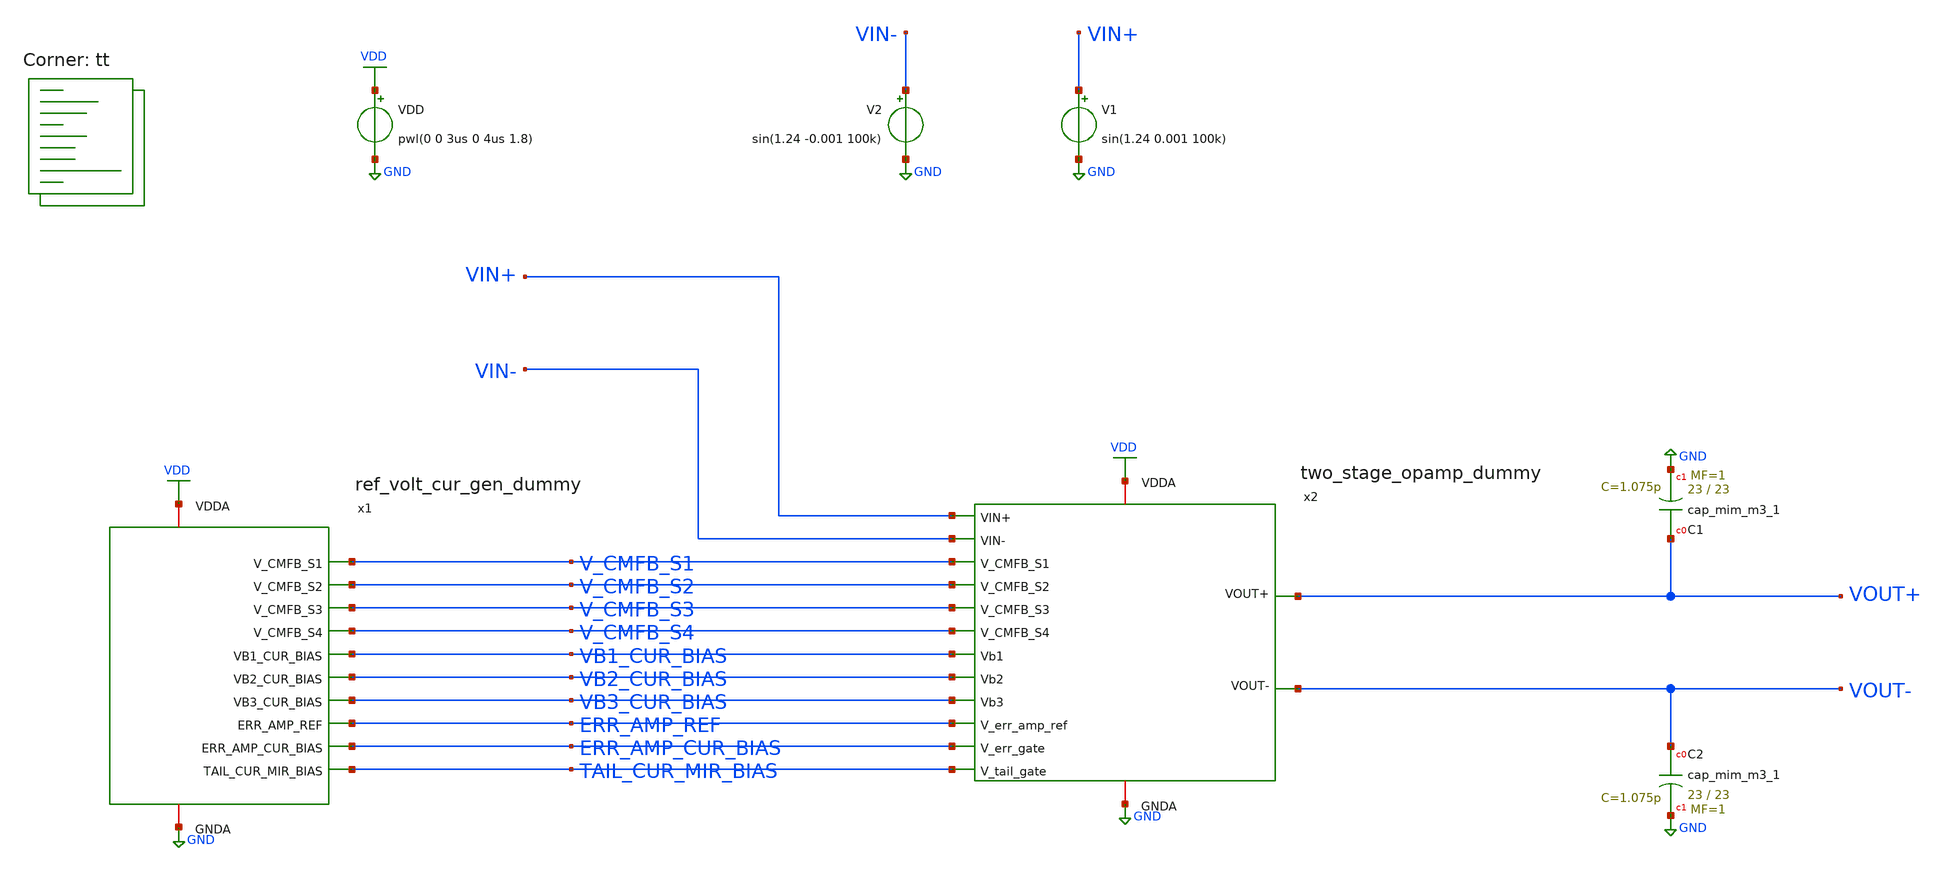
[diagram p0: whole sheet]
** sch_path: projects/opamp/xschem_ngspice/tb_two_stage_opamp_dummy.sch
**.subckt tb_two_stage_opamp_dummy
VDD VDD GND pwl(0 0 3us 0 4us 1.8)
V2 VIN- GND sin(1.24 -0.001 100k)
V1 VIN+ GND sin(1.24 0.001 100k)
XC1 VOUT+ GND sky130_fd_pr__cap_mim_m3_1 W=23 L=23 MF=1 m=1
XC2 VOUT- GND sky130_fd_pr__cap_mim_m3_1 W=23 L=23 MF=1 m=1
x1 VDD ERR_AMP_REF V_CMFB_S3 VB1_CUR_BIAS TAIL_CUR_MIR_BIAS V_CMFB_S1 ERR_AMP_CUR_BIAS VB3_CUR_BIAS
+ V_CMFB_S4 V_CMFB_S2 VB2_CUR_BIAS GND ref_volt_cur_gen_dummy
x2 VDD V_CMFB_S1 V_CMFB_S3 VB3_CUR_BIAS VB2_CUR_BIAS VB1_CUR_BIAS V_CMFB_S2 V_CMFB_S4 VOUT- VOUT+
+ TAIL_CUR_MIR_BIAS ERR_AMP_REF ERR_AMP_CUR_BIAS VIN+ VIN- GND two_stage_opamp_dummy
**** begin user architecture code
.lib $::SKYWATER_MODELS/sky130.lib.spice tt




.option method=gear
.option wnflag=1
.option savecurrents

.save @m.x1.xm1.msky130_fd_pr__pfet_01v8[gm] @m.x1.xm1.msky130_fd_pr__pfet_01v8[vth] @m.x1.xm2.msky130_fd_pr__pfet_01v8[gm] @m.x1.xm2.msky130_fd_pr__pfet_01v8[vth] @m.x1.xm3.msky130_fd_pr__pfet_01v8[gm] @m.x1.xm3.msky130_fd_pr__pfet_01v8[vth] @m.x1.xm4.msky130_fd_pr__pfet_01v8[gm] @m.x1.xm4.msky130_fd_pr__pfet_01v8[vth] @m.x1.xm5.msky130_fd_pr__nfet_01v8[gm] @m.x1.xm5.msky130_fd_pr__nfet_01v8[vth] @m.x1.xm6.msky130_fd_pr__pfet_01v8[gm] @m.x1.xm6.msky130_fd_pr__pfet_01v8[vth] @m.x1.xm7.msky130_fd_pr__nfet_01v8[gm] @m.x1.xm7.msky130_fd_pr__nfet_01v8[vth] @m.x1.xm8.msky130_fd_pr__pfet_01v8[gm] @m.x1.xm8.msky130_fd_pr__pfet_01v8[vth] @m.x2.xm2.msky130_fd_pr__nfet_01v8[gm] @m.x2.xm2.msky130_fd_pr__nfet_01v8[vth] @m.x2.xm3.msky130_fd_pr__nfet_01v8[gm] @m.x2.xm3.msky130_fd_pr__nfet_01v8[vth] @m.x2.xm7.msky130_fd_pr__pfet_01v8[gm] @m.x2.xm7.msky130_fd_pr__pfet_01v8[vth] @m.x1.x1.xm1.msky130_fd_pr__nfet_01v8[gm] @m.x1.x1.xm2.msky130_fd_pr__nfet_01v8[gm] @m.x1.x1.xm3.msky130_fd_pr__nfet_01v8[gm] @m.x1.x1.xm4.msky130_fd_pr__nfet_01v8[gm] @m.x1.x1.xm5.msky130_fd_pr__pfet_01v8[gm] @m.x1.x1.xm6.msky130_fd_pr__nfet_01v8[gm] @m.x1.x1.xm7.msky130_fd_pr__pfet_01v8[gm] @m.x1.x2.xm1.msky130_fd_pr__nfet_01v8[gm] @m.x1.x2.xm2.msky130_fd_pr__nfet_01v8[gm] @m.x1.x2.xm3.msky130_fd_pr__nfet_01v8[gm] @m.x1.x2.xm4.msky130_fd_pr__nfet_01v8[gm] @m.x1.x2.xm5.msky130_fd_pr__pfet_01v8[gm] @m.x1.x2.xm6.msky130_fd_pr__nfet_01v8[gm] @m.x1.x2.xm7.msky130_fd_pr__pfet_01v8[gm] @m.x2.xm39.msky130_fd_pr__pfet_01v8[gm] @m.x2.xm39.msky130_fd_pr__pfet_01v8[vth] @m.x2.xm40.msky130_fd_pr__pfet_01v8[gm] @m.x2.xm40.msky130_fd_pr__pfet_01v8[vth]

* .ic v(v_top) = 1.8

.control

  * let runs=3
  * let run=1

  * dowhile run <= runs
    * save v(vout+) v(vout-) v(vin+) v(vin-) v(v_err_amp_ref) v(x2.x) v(x2.y) v(x2.vb1) v(x2.vb2)
+ v(x2.vb3) v(x2.v_tot)
    save all
    remzerovec
    set appendwrite
    * dc temp -40 120 10 VDD 0 4.0 0.2
    * dc VDD 0 2.0 0.02 temp -40 120 40
    * dc V5 0 0.01 0.0001
    tran 2n 30u
    * tran 1p 3n
    * tran 0.1ns 30us
    * ac dec 40 1 10T
    write tb_two_stage_opamp_dummy.raw
    * write tb_two_stage_opamp_dummy_mc.raw
    * write tb_two_stage_opamp_dummy_tt_mm.raw
    * write tb_two_stage_opamp_dummy_AC.raw
    * reset
    * let run = run + 1
  * end
.endc




**** end user architecture code
**.ends

* expanding   symbol:  ref_volt_cur_gen_dummy.sym # of pins=12
** sym_path: projects/opamp/xschem_ngspice/ref_volt_cur_gen_dummy.sym
** sch_path: projects/opamp/xschem_ngspice/ref_volt_cur_gen_dummy.sch
.subckt ref_volt_cur_gen_dummy VDDA ERR_AMP_REF V_CMFB_S3 VB1_CUR_BIAS TAIL_CUR_MIR_BIAS V_CMFB_S1
+ ERR_AMP_CUR_BIAS VB3_CUR_BIAS V_CMFB_S4 V_CMFB_S2 VB2_CUR_BIAS GNDA
*.opin VB1_CUR_BIAS
*.iopin GNDA
*.opin ERR_AMP_REF
*.iopin VDDA
*.opin VB2_CUR_BIAS
*.opin VB3_CUR_BIAS
*.opin ERR_AMP_CUR_BIAS
*.opin V_CMFB_S2
*.opin TAIL_CUR_MIR_BIAS
*.opin V_CMFB_S1
*.opin V_CMFB_S4
*.opin V_CMFB_S3
XM3 ERR_AMP_REF V_TOP VDDA VDDA sky130_fd_pr__pfet_01v8 L=0.5 W=12 nf=4 ad='int((nf+1)/2) * W/nf * 0.29'
+ as='int((nf+2)/2) * W/nf * 0.29' pd='2*int((nf+1)/2) * (W/nf + 0.29)' ps='2*int((nf+2)/2) * (W/nf + 0.29)'
+ nrd='0.29 / W' nrs='0.29 / W' sa=0 sb=0 sd=0 mult=1 m=1
XR4 GNDA ERR_AMP_REF GNDA sky130_fd_pr__res_xhigh_po_0p35 L=12.7 mult=1 m=1
XR5 GNDA V_CUR_REF_REG GNDA sky130_fd_pr__res_xhigh_po_0p35 L=12 mult=1 m=1
XM8 V_CUR_REF_REG PFET_GATE_10uA VDDA VDDA sky130_fd_pr__pfet_01v8 L=0.15 W=1 nf=1 ad='int((nf+1)/2) * W/nf * 0.29'
+ as='int((nf+2)/2) * W/nf * 0.29' pd='2*int((nf+1)/2) * (W/nf + 0.29)' ps='2*int((nf+2)/2) * (W/nf + 0.29)'
+ nrd='0.29 / W' nrs='0.29 / W' sa=0 sb=0 sd=0 mult=1 m=1
XC1 V_TOP VDDA sky130_fd_pr__cap_mim_m3_1 W=2 L=2 MF=20 m=20
XQ1 GNDA GNDA Vin- sky130_fd_pr__pnp_05v5_W3p40L3p40 m=1
XQ2 GNDA GNDA Vbe2 sky130_fd_pr__pnp_05v5_W3p40L3p40 m=8
XM1 Vin- V_TOP VDDA VDDA sky130_fd_pr__pfet_01v8 L=0.5 W=12 nf=4 ad='int((nf+1)/2) * W/nf * 0.29' as='int((nf+2)/2) * W/nf * 0.29'
+ pd='2*int((nf+1)/2) * (W/nf + 0.29)' ps='2*int((nf+2)/2) * (W/nf + 0.29)' nrd='0.29 / W' nrs='0.29 / W'
+ sa=0 sb=0 sd=0 mult=1 m=1
XM2 Vin+ V_TOP VDDA VDDA sky130_fd_pr__pfet_01v8 L=0.5 W=12 nf=4 ad='int((nf+1)/2) * W/nf * 0.29' as='int((nf+2)/2) * W/nf * 0.29'
+ pd='2*int((nf+1)/2) * (W/nf + 0.29)' ps='2*int((nf+2)/2) * (W/nf + 0.29)' nrd='0.29 / W' nrs='0.29 / W'
+ sa=0 sb=0 sd=0 mult=1 m=1
XR1 Vbe2 Vin+ GNDA sky130_fd_pr__res_xhigh_po_0p35 L=2.3 mult=1 m=1
XR3 GNDA Vin+ GNDA sky130_fd_pr__res_xhigh_po_0p35 L=18 mult=1 m=1
XR2 GNDA Vin- GNDA sky130_fd_pr__res_xhigh_po_0p35 L=18 mult=1 m=1
XM6 START_UP START_UP START_UP_NFET1 GNDA sky130_fd_pr__nfet_01v8 L=10 W=1 nf=1 ad='int((nf+1)/2) * W/nf * 0.29'
+ as='int((nf+2)/2) * W/nf * 0.29' pd='2*int((nf+1)/2) * (W/nf + 0.29)' ps='2*int((nf+2)/2) * (W/nf + 0.29)'
+ nrd='0.29 / W' nrs='0.29 / W' sa=0 sb=0 sd=0 mult=1 m=1
XM4 START_UP V_TOP VDDA VDDA sky130_fd_pr__pfet_01v8 L=0.5 W=12 nf=4 ad='int((nf+1)/2) * W/nf * 0.29'
+ as='int((nf+2)/2) * W/nf * 0.29' pd='2*int((nf+1)/2) * (W/nf + 0.29)' ps='2*int((nf+2)/2) * (W/nf + 0.29)'
+ nrd='0.29 / W' nrs='0.29 / W' sa=0 sb=0 sd=0 mult=1 m=1
XM5 Vin- START_UP V_TOP VDDA sky130_fd_pr__pfet_01v8 L=0.15 W=2 nf=2 ad='int((nf+1)/2) * W/nf * 0.29'
+ as='int((nf+2)/2) * W/nf * 0.29' pd='2*int((nf+1)/2) * (W/nf + 0.29)' ps='2*int((nf+2)/2) * (W/nf + 0.29)'
+ nrd='0.29 / W' nrs='0.29 / W' sa=0 sb=0 sd=0 mult=1 m=1
XM7 START_UP_NFET1 START_UP_NFET1 GNDA GNDA sky130_fd_pr__nfet_01v8 L=10 W=1 nf=1 ad='int((nf+1)/2) * W/nf * 0.29'
+ as='int((nf+2)/2) * W/nf * 0.29' pd='2*int((nf+1)/2) * (W/nf + 0.29)' ps='2*int((nf+2)/2) * (W/nf + 0.29)'
+ nrd='0.29 / W' nrs='0.29 / W' sa=0 sb=0 sd=0 mult=1 m=1
x1 VDDA V_TOP Vin- Vin+ GNDA opamp_bandgap_2
x2 VDDA PFET_GATE_10uA ERR_AMP_REF V_CUR_REF_REG GNDA opamp_bandgap_2
XM9 NFET_GATE_10uA PFET_GATE_10uA VDDA VDDA sky130_fd_pr__pfet_01v8 L=0.15 W=1 nf=1 ad='int((nf+1)/2) * W/nf * 0.29'
+ as='int((nf+2)/2) * W/nf * 0.29' pd='2*int((nf+1)/2) * (W/nf + 0.29)' ps='2*int((nf+2)/2) * (W/nf + 0.29)'
+ nrd='0.29 / W' nrs='0.29 / W' sa=0 sb=0 sd=0 mult=1 m=1
XM10 NFET_GATE_10uA NFET_GATE_10uA GNDA GNDA sky130_fd_pr__nfet_01v8 L=0.15 W=1 nf=1 ad='int((nf+1)/2) * W/nf * 0.29'
+ as='int((nf+2)/2) * W/nf * 0.29' pd='2*int((nf+1)/2) * (W/nf + 0.29)' ps='2*int((nf+2)/2) * (W/nf + 0.29)'
+ nrd='0.29 / W' nrs='0.29 / W' sa=0 sb=0 sd=0 mult=1 m=1
XM11 VB2_CUR_BIAS NFET_GATE_10uA GNDA GNDA sky130_fd_pr__nfet_01v8 L=0.15 W=1 nf=1 ad='int((nf+1)/2) * W/nf * 0.29'
+ as='int((nf+2)/2) * W/nf * 0.29' pd='2*int((nf+1)/2) * (W/nf + 0.29)' ps='2*int((nf+2)/2) * (W/nf + 0.29)'
+ nrd='0.29 / W' nrs='0.29 / W' sa=0 sb=0 sd=0 mult=6 m=6
XM12 VB3_CUR_BIAS NFET_GATE_10uA GNDA GNDA sky130_fd_pr__nfet_01v8 L=0.15 W=1 nf=1 ad='int((nf+1)/2) * W/nf * 0.29'
+ as='int((nf+2)/2) * W/nf * 0.29' pd='2*int((nf+1)/2) * (W/nf + 0.29)' ps='2*int((nf+2)/2) * (W/nf + 0.29)'
+ nrd='0.29 / W' nrs='0.29 / W' sa=0 sb=0 sd=0 mult=5 m=5
XM30 VB1_CUR_BIAS PFET_GATE_10uA VDDA VDDA sky130_fd_pr__pfet_01v8 L=0.15 W=1 nf=1 ad='int((nf+1)/2) * W/nf * 0.29'
+ as='int((nf+2)/2) * W/nf * 0.29' pd='2*int((nf+1)/2) * (W/nf + 0.29)' ps='2*int((nf+2)/2) * (W/nf + 0.29)'
+ nrd='0.29 / W' nrs='0.29 / W' sa=0 sb=0 sd=0 mult=2 m=2
XM13 ERR_AMP_CUR_BIAS NFET_GATE_10uA GNDA GNDA sky130_fd_pr__nfet_01v8 L=0.15 W=1 nf=1 ad='int((nf+1)/2) * W/nf * 0.29'
+ as='int((nf+2)/2) * W/nf * 0.29' pd='2*int((nf+1)/2) * (W/nf + 0.29)' ps='2*int((nf+2)/2) * (W/nf + 0.29)'
+ nrd='0.29 / W' nrs='0.29 / W' sa=0 sb=0 sd=0 mult=2 m=2
XM14 V_CMFB_S2 NFET_GATE_10uA GNDA GNDA sky130_fd_pr__nfet_01v8 L=0.15 W=1 nf=1 ad='int((nf+1)/2) * W/nf * 0.29'
+ as='int((nf+2)/2) * W/nf * 0.29' pd='2*int((nf+1)/2) * (W/nf + 0.29)' ps='2*int((nf+2)/2) * (W/nf + 0.29)'
+ nrd='0.29 / W' nrs='0.29 / W' sa=0 sb=0 sd=0 mult=3 m=3
XM16 TAIL_CUR_MIR_BIAS PFET_GATE_10uA VDDA VDDA sky130_fd_pr__pfet_01v8 L=0.15 W=1 nf=1 ad='int((nf+1)/2) * W/nf * 0.29'
+ as='int((nf+2)/2) * W/nf * 0.29' pd='2*int((nf+1)/2) * (W/nf + 0.29)' ps='2*int((nf+2)/2) * (W/nf + 0.29)'
+ nrd='0.29 / W' nrs='0.29 / W' sa=0 sb=0 sd=0 mult=8 m=8
XM17 NFET_GATE_10uA VDDA VDDA VDDA sky130_fd_pr__pfet_01v8 L=0.15 W=1 nf=1 ad='int((nf+1)/2) * W/nf * 0.29'
+ as='int((nf+2)/2) * W/nf * 0.29' pd='2*int((nf+1)/2) * (W/nf + 0.29)' ps='2*int((nf+2)/2) * (W/nf + 0.29)'
+ nrd='0.29 / W' nrs='0.29 / W' sa=0 sb=0 sd=0 mult=1 m=1
XM18 NFET_GATE_10uA GNDA GNDA GNDA sky130_fd_pr__nfet_01v8 L=0.15 W=1 nf=1 ad='int((nf+1)/2) * W/nf * 0.29'
+ as='int((nf+2)/2) * W/nf * 0.29' pd='2*int((nf+1)/2) * (W/nf + 0.29)' ps='2*int((nf+2)/2) * (W/nf + 0.29)'
+ nrd='0.29 / W' nrs='0.29 / W' sa=0 sb=0 sd=0 mult=1 m=1
XM19 V_CUR_REF_REG VDDA VDDA VDDA sky130_fd_pr__pfet_01v8 L=0.15 W=1 nf=1 ad='int((nf+1)/2) * W/nf * 0.29'
+ as='int((nf+2)/2) * W/nf * 0.29' pd='2*int((nf+1)/2) * (W/nf + 0.29)' ps='2*int((nf+2)/2) * (W/nf + 0.29)'
+ nrd='0.29 / W' nrs='0.29 / W' sa=0 sb=0 sd=0 mult=1 m=1
XM20 VB3_CUR_BIAS GNDA GNDA GNDA sky130_fd_pr__nfet_01v8 L=0.15 W=1 nf=1 ad='int((nf+1)/2) * W/nf * 0.29'
+ as='int((nf+2)/2) * W/nf * 0.29' pd='2*int((nf+1)/2) * (W/nf + 0.29)' ps='2*int((nf+2)/2) * (W/nf + 0.29)'
+ nrd='0.29 / W' nrs='0.29 / W' sa=0 sb=0 sd=0 mult=1 m=1
XM28 V_CMFB_S1 PFET_GATE_10uA VDDA VDDA sky130_fd_pr__pfet_01v8 L=0.15 W=1 nf=1 ad='int((nf+1)/2) * W/nf * 0.29'
+ as='int((nf+2)/2) * W/nf * 0.29' pd='2*int((nf+1)/2) * (W/nf + 0.29)' ps='2*int((nf+2)/2) * (W/nf + 0.29)'
+ nrd='0.29 / W' nrs='0.29 / W' sa=0 sb=0 sd=0 mult=4 m=4
XM22 ERR_AMP_REF VDDA VDDA VDDA sky130_fd_pr__pfet_01v8 L=0.5 W=6 nf=2 ad='int((nf+1)/2) * W/nf * 0.29'
+ as='int((nf+2)/2) * W/nf * 0.29' pd='2*int((nf+1)/2) * (W/nf + 0.29)' ps='2*int((nf+2)/2) * (W/nf + 0.29)'
+ nrd='0.29 / W' nrs='0.29 / W' sa=0 sb=0 sd=0 mult=1 m=1
XM23 V_CMFB_S4 NFET_GATE_10uA GNDA GNDA sky130_fd_pr__nfet_01v8 L=0.15 W=1 nf=1 ad='int((nf+1)/2) * W/nf * 0.29'
+ as='int((nf+2)/2) * W/nf * 0.29' pd='2*int((nf+1)/2) * (W/nf + 0.29)' ps='2*int((nf+2)/2) * (W/nf + 0.29)'
+ nrd='0.29 / W' nrs='0.29 / W' sa=0 sb=0 sd=0 mult=3 m=3
XM29 V_CMFB_S3 PFET_GATE_10uA VDDA VDDA sky130_fd_pr__pfet_01v8 L=0.15 W=1 nf=1 ad='int((nf+1)/2) * W/nf * 0.29'
+ as='int((nf+2)/2) * W/nf * 0.29' pd='2*int((nf+1)/2) * (W/nf + 0.29)' ps='2*int((nf+2)/2) * (W/nf + 0.29)'
+ nrd='0.29 / W' nrs='0.29 / W' sa=0 sb=0 sd=0 mult=4 m=4
XM25 V_CMFB_S2 GNDA GNDA GNDA sky130_fd_pr__nfet_01v8 L=0.15 W=1 nf=1 ad='int((nf+1)/2) * W/nf * 0.29'
+ as='int((nf+2)/2) * W/nf * 0.29' pd='2*int((nf+1)/2) * (W/nf + 0.29)' ps='2*int((nf+2)/2) * (W/nf + 0.29)'
+ nrd='0.29 / W' nrs='0.29 / W' sa=0 sb=0 sd=0 mult=1 m=1
XM26 V_CMFB_S4 GNDA GNDA GNDA sky130_fd_pr__nfet_01v8 L=0.15 W=1 nf=1 ad='int((nf+1)/2) * W/nf * 0.29'
+ as='int((nf+2)/2) * W/nf * 0.29' pd='2*int((nf+1)/2) * (W/nf + 0.29)' ps='2*int((nf+2)/2) * (W/nf + 0.29)'
+ nrd='0.29 / W' nrs='0.29 / W' sa=0 sb=0 sd=0 mult=1 m=1
XM27 VB2_CUR_BIAS GNDA GNDA GNDA sky130_fd_pr__nfet_01v8 L=0.15 W=1 nf=1 ad='int((nf+1)/2) * W/nf * 0.29'
+ as='int((nf+2)/2) * W/nf * 0.29' pd='2*int((nf+1)/2) * (W/nf + 0.29)' ps='2*int((nf+2)/2) * (W/nf + 0.29)'
+ nrd='0.29 / W' nrs='0.29 / W' sa=0 sb=0 sd=0 mult=2 m=2
XM21 V_CMFB_S1 VDDA VDDA VDDA sky130_fd_pr__pfet_01v8 L=0.15 W=1 nf=1 ad='int((nf+1)/2) * W/nf * 0.29'
+ as='int((nf+2)/2) * W/nf * 0.29' pd='2*int((nf+1)/2) * (W/nf + 0.29)' ps='2*int((nf+2)/2) * (W/nf + 0.29)'
+ nrd='0.29 / W' nrs='0.29 / W' sa=0 sb=0 sd=0 mult=2 m=2
XM24 V_CMFB_S3 VDDA VDDA VDDA sky130_fd_pr__pfet_01v8 L=0.15 W=1 nf=1 ad='int((nf+1)/2) * W/nf * 0.29'
+ as='int((nf+2)/2) * W/nf * 0.29' pd='2*int((nf+1)/2) * (W/nf + 0.29)' ps='2*int((nf+2)/2) * (W/nf + 0.29)'
+ nrd='0.29 / W' nrs='0.29 / W' sa=0 sb=0 sd=0 mult=2 m=2
XM15 VB1_CUR_BIAS VDDA VDDA VDDA sky130_fd_pr__pfet_01v8 L=0.15 W=1 nf=1 ad='int((nf+1)/2) * W/nf * 0.29'
+ as='int((nf+2)/2) * W/nf * 0.29' pd='2*int((nf+1)/2) * (W/nf + 0.29)' ps='2*int((nf+2)/2) * (W/nf + 0.29)'
+ nrd='0.29 / W' nrs='0.29 / W' sa=0 sb=0 sd=0 mult=2 m=2
XM31 V_TOP VDDA VDDA VDDA sky130_fd_pr__pfet_01v8 L=0.15 W=2 nf=2 ad='int((nf+1)/2) * W/nf * 0.29' as='int((nf+2)/2) * W/nf * 0.29'
+ pd='2*int((nf+1)/2) * (W/nf + 0.29)' ps='2*int((nf+2)/2) * (W/nf + 0.29)' nrd='0.29 / W' nrs='0.29 / W'
+ sa=0 sb=0 sd=0 mult=1 m=1
.ends


* expanding   symbol:  two_stage_opamp_dummy.sym # of pins=16
** sym_path: projects/opamp/xschem_ngspice/two_stage_opamp_dummy.sym
** sch_path: projects/opamp/xschem_ngspice/two_stage_opamp_dummy.sch
.subckt two_stage_opamp_dummy VDDA V_CMFB_S1 V_CMFB_S3 Vb3 Vb2 Vb1 V_CMFB_S2 V_CMFB_S4 VOUT- VOUT+
+ V_tail_gate V_err_amp_ref V_err_gate VIN+ VIN- GNDA
*.iopin VDDA
*.ipin V_err_amp_ref
*.iopin GNDA
*.ipin VIN-
*.ipin VIN+
*.opin VOUT+
*.opin VOUT-
*.ipin Vb2
*.ipin Vb3
*.ipin V_tail_gate
*.ipin Vb1
*.ipin V_err_gate
*.ipin V_CMFB_S1
*.ipin V_CMFB_S3
*.ipin V_CMFB_S2
*.ipin V_CMFB_S4
XM7 VD1 VIN- V_p GNDA sky130_fd_pr__nfet_01v8 L=0.15 W=15 nf=1 ad='int((nf+1)/2) * W/nf * 0.29' as='int((nf+2)/2) * W/nf * 0.29'
+ pd='2*int((nf+1)/2) * (W/nf + 0.29)' ps='2*int((nf+2)/2) * (W/nf + 0.29)' nrd='0.29 / W' nrs='0.29 / W'
+ sa=0 sb=0 sd=0 mult=1 m=1
XM8 VD2 VIN+ V_p GNDA sky130_fd_pr__nfet_01v8 L=0.15 W=15 nf=1 ad='int((nf+1)/2) * W/nf * 0.29' as='int((nf+2)/2) * W/nf * 0.29'
+ pd='2*int((nf+1)/2) * (W/nf + 0.29)' ps='2*int((nf+2)/2) * (W/nf + 0.29)' nrd='0.29 / W' nrs='0.29 / W'
+ sa=0 sb=0 sd=0 mult=1 m=1
XM9 X Vb1 VD1 GNDA sky130_fd_pr__nfet_01v8 L=0.15 W=15 nf=1 ad='int((nf+1)/2) * W/nf * 0.29' as='int((nf+2)/2) * W/nf * 0.29'
+ pd='2*int((nf+1)/2) * (W/nf + 0.29)' ps='2*int((nf+2)/2) * (W/nf + 0.29)' nrd='0.29 / W' nrs='0.29 / W'
+ sa=0 sb=0 sd=0 mult=1 m=1
XM10 Y Vb1 VD2 GNDA sky130_fd_pr__nfet_01v8 L=0.15 W=15 nf=1 ad='int((nf+1)/2) * W/nf * 0.29' as='int((nf+2)/2) * W/nf * 0.29'
+ pd='2*int((nf+1)/2) * (W/nf + 0.29)' ps='2*int((nf+2)/2) * (W/nf + 0.29)' nrd='0.29 / W' nrs='0.29 / W'
+ sa=0 sb=0 sd=0 mult=1 m=1
XM11 X Vb2 VD3 VD3 sky130_fd_pr__pfet_01v8 L=0.2 W=35 nf=1 ad='int((nf+1)/2) * W/nf * 0.29' as='int((nf+2)/2) * W/nf * 0.29'
+ pd='2*int((nf+1)/2) * (W/nf + 0.29)' ps='2*int((nf+2)/2) * (W/nf + 0.29)' nrd='0.29 / W' nrs='0.29 / W'
+ sa=0 sb=0 sd=0 mult=1 m=1
XM12 Y Vb2 VD4 VD4 sky130_fd_pr__pfet_01v8 L=0.2 W=35 nf=1 ad='int((nf+1)/2) * W/nf * 0.29' as='int((nf+2)/2) * W/nf * 0.29'
+ pd='2*int((nf+1)/2) * (W/nf + 0.29)' ps='2*int((nf+2)/2) * (W/nf + 0.29)' nrd='0.29 / W' nrs='0.29 / W'
+ sa=0 sb=0 sd=0 mult=1 m=1
XM13 VD3 Vb3 VDDA VDDA sky130_fd_pr__pfet_01v8 L=0.2 W=35 nf=1 ad='int((nf+1)/2) * W/nf * 0.29' as='int((nf+2)/2) * W/nf * 0.29'
+ pd='2*int((nf+1)/2) * (W/nf + 0.29)' ps='2*int((nf+2)/2) * (W/nf + 0.29)' nrd='0.29 / W' nrs='0.29 / W'
+ sa=0 sb=0 sd=0 mult=1 m=1
XM14 VD4 Vb3 VDDA VDDA sky130_fd_pr__pfet_01v8 L=0.2 W=35 nf=1 ad='int((nf+1)/2) * W/nf * 0.29' as='int((nf+2)/2) * W/nf * 0.29'
+ pd='2*int((nf+1)/2) * (W/nf + 0.29)' ps='2*int((nf+2)/2) * (W/nf + 0.29)' nrd='0.29 / W' nrs='0.29 / W'
+ sa=0 sb=0 sd=0 mult=1 m=1
XM15 V_p V_tail_gate GNDA GNDA sky130_fd_pr__nfet_01v8 L=0.15 W=45 nf=1 ad='int((nf+1)/2) * W/nf * 0.29'
+ as='int((nf+2)/2) * W/nf * 0.29' pd='2*int((nf+1)/2) * (W/nf + 0.29)' ps='2*int((nf+2)/2) * (W/nf + 0.29)'
+ nrd='0.29 / W' nrs='0.29 / W' sa=0 sb=0 sd=0 mult=1 m=1
XM16 V_p_mir V_tail_gate GNDA GNDA sky130_fd_pr__nfet_01v8 L=0.15 W=5 nf=1 ad='int((nf+1)/2) * W/nf * 0.29'
+ as='int((nf+2)/2) * W/nf * 0.29' pd='2*int((nf+1)/2) * (W/nf + 0.29)' ps='2*int((nf+2)/2) * (W/nf + 0.29)'
+ nrd='0.29 / W' nrs='0.29 / W' sa=0 sb=0 sd=0 mult=1 m=1
XM17 V_tail_gate VIN+ V_p_mir GNDA sky130_fd_pr__nfet_01v8 L=0.15 W=1.5 nf=1 ad='int((nf+1)/2) * W/nf * 0.29'
+ as='int((nf+2)/2) * W/nf * 0.29' pd='2*int((nf+1)/2) * (W/nf + 0.29)' ps='2*int((nf+2)/2) * (W/nf + 0.29)'
+ nrd='0.29 / W' nrs='0.29 / W' sa=0 sb=0 sd=0 mult=1 m=1
XM18 V_tail_gate VIN- V_p_mir GNDA sky130_fd_pr__nfet_01v8 L=0.15 W=1.5 nf=1 ad='int((nf+1)/2) * W/nf * 0.29'
+ as='int((nf+2)/2) * W/nf * 0.29' pd='2*int((nf+1)/2) * (W/nf + 0.29)' ps='2*int((nf+2)/2) * (W/nf + 0.29)'
+ nrd='0.29 / W' nrs='0.29 / W' sa=0 sb=0 sd=0 mult=1 m=1
XM19 Vb1 Vb1 V_p GNDA sky130_fd_pr__nfet_01v8 L=2.9 W=1 nf=1 ad='int((nf+1)/2) * W/nf * 0.29' as='int((nf+2)/2) * W/nf * 0.29'
+ pd='2*int((nf+1)/2) * (W/nf + 0.29)' ps='2*int((nf+2)/2) * (W/nf + 0.29)' nrd='0.29 / W' nrs='0.29 / W'
+ sa=0 sb=0 sd=0 mult=1 m=1
XM25 VDDA X V_CMFB_S2 GNDA sky130_fd_pr__nfet_01v8 L=0.15 W=30 nf=1 ad='int((nf+1)/2) * W/nf * 0.29'
+ as='int((nf+2)/2) * W/nf * 0.29' pd='2*int((nf+1)/2) * (W/nf + 0.29)' ps='2*int((nf+2)/2) * (W/nf + 0.29)'
+ nrd='0.29 / W' nrs='0.29 / W' sa=0 sb=0 sd=0 mult=1 m=1
XM26 GNDA X V_CMFB_S1 VDDA sky130_fd_pr__pfet_01v8 L=0.15 W=20 nf=1 ad='int((nf+1)/2) * W/nf * 0.29'
+ as='int((nf+2)/2) * W/nf * 0.29' pd='2*int((nf+1)/2) * (W/nf + 0.29)' ps='2*int((nf+2)/2) * (W/nf + 0.29)'
+ nrd='0.29 / W' nrs='0.29 / W' sa=0 sb=0 sd=0 mult=1 m=1
XR10 V_CMFB_S1 V_tot GNDA sky130_fd_pr__res_xhigh_po_0p35 L=3.5 mult=1 m=1
XR11 V_CMFB_S2 V_tot GNDA sky130_fd_pr__res_xhigh_po_0p35 L=3.5 mult=1 m=1
XR12 V_CMFB_S3 V_tot GNDA sky130_fd_pr__res_xhigh_po_0p35 L=3.5 mult=1 m=1
XR13 V_CMFB_S4 V_tot GNDA sky130_fd_pr__res_xhigh_po_0p35 L=3.5 mult=1 m=1
XM27 VDDA Y V_CMFB_S4 GNDA sky130_fd_pr__nfet_01v8 L=0.15 W=30 nf=1 ad='int((nf+1)/2) * W/nf * 0.29'
+ as='int((nf+2)/2) * W/nf * 0.29' pd='2*int((nf+1)/2) * (W/nf + 0.29)' ps='2*int((nf+2)/2) * (W/nf + 0.29)'
+ nrd='0.29 / W' nrs='0.29 / W' sa=0 sb=0 sd=0 mult=1 m=1
XM28 GNDA Y V_CMFB_S3 VDDA sky130_fd_pr__pfet_01v8 L=0.15 W=20 nf=1 ad='int((nf+1)/2) * W/nf * 0.29'
+ as='int((nf+2)/2) * W/nf * 0.29' pd='2*int((nf+1)/2) * (W/nf + 0.29)' ps='2*int((nf+2)/2) * (W/nf + 0.29)'
+ nrd='0.29 / W' nrs='0.29 / W' sa=0 sb=0 sd=0 mult=1 m=1
XM29 err_amp_mir V_tot V_err_p VDDA sky130_fd_pr__pfet_01v8 L=0.15 W=2.5 nf=1 ad='int((nf+1)/2) * W/nf * 0.29'
+ as='int((nf+2)/2) * W/nf * 0.29' pd='2*int((nf+1)/2) * (W/nf + 0.29)' ps='2*int((nf+2)/2) * (W/nf + 0.29)'
+ nrd='0.29 / W' nrs='0.29 / W' sa=0 sb=0 sd=0 mult=1 m=1
XM30 err_amp_out V_err_amp_ref V_err_p VDDA sky130_fd_pr__pfet_01v8 L=0.15 W=2.5 nf=1 ad='int((nf+1)/2) * W/nf * 0.29'
+ as='int((nf+2)/2) * W/nf * 0.29' pd='2*int((nf+1)/2) * (W/nf + 0.29)' ps='2*int((nf+2)/2) * (W/nf + 0.29)'
+ nrd='0.29 / W' nrs='0.29 / W' sa=0 sb=0 sd=0 mult=1 m=1
XM31 err_amp_mir err_amp_mir GNDA GNDA sky130_fd_pr__nfet_01v8 L=0.15 W=2.5 nf=1 ad='int((nf+1)/2) * W/nf * 0.29'
+ as='int((nf+2)/2) * W/nf * 0.29' pd='2*int((nf+1)/2) * (W/nf + 0.29)' ps='2*int((nf+2)/2) * (W/nf + 0.29)'
+ nrd='0.29 / W' nrs='0.29 / W' sa=0 sb=0 sd=0 mult=1 m=1
XM32 err_amp_out err_amp_mir GNDA GNDA sky130_fd_pr__nfet_01v8 L=0.15 W=2.5 nf=1 ad='int((nf+1)/2) * W/nf * 0.29'
+ as='int((nf+2)/2) * W/nf * 0.29' pd='2*int((nf+1)/2) * (W/nf + 0.29)' ps='2*int((nf+2)/2) * (W/nf + 0.29)'
+ nrd='0.29 / W' nrs='0.29 / W' sa=0 sb=0 sd=0 mult=1 m=1
XM33 V_err_p V_err_gate VDDA VDDA sky130_fd_pr__pfet_01v8 L=0.15 W=5.0 nf=2 ad='int((nf+1)/2) * W/nf * 0.29'
+ as='int((nf+2)/2) * W/nf * 0.29' pd='2*int((nf+1)/2) * (W/nf + 0.29)' ps='2*int((nf+2)/2) * (W/nf + 0.29)'
+ nrd='0.29 / W' nrs='0.29 / W' sa=0 sb=0 sd=0 mult=1 m=1
XM34 V_err_gate V_tot V_err_mir_p VDDA sky130_fd_pr__pfet_01v8 L=0.15 W=2.5 nf=1 ad='int((nf+1)/2) * W/nf * 0.29'
+ as='int((nf+2)/2) * W/nf * 0.29' pd='2*int((nf+1)/2) * (W/nf + 0.29)' ps='2*int((nf+2)/2) * (W/nf + 0.29)'
+ nrd='0.29 / W' nrs='0.29 / W' sa=0 sb=0 sd=0 mult=1 m=1
XM35 V_err_gate V_err_amp_ref V_err_mir_p VDDA sky130_fd_pr__pfet_01v8 L=0.15 W=2.5 nf=1 ad='int((nf+1)/2) * W/nf * 0.29'
+ as='int((nf+2)/2) * W/nf * 0.29' pd='2*int((nf+1)/2) * (W/nf + 0.29)' ps='2*int((nf+2)/2) * (W/nf + 0.29)'
+ nrd='0.29 / W' nrs='0.29 / W' sa=0 sb=0 sd=0 mult=1 m=1
XM36 V_err_mir_p V_err_gate VDDA VDDA sky130_fd_pr__pfet_01v8 L=0.15 W=5.0 nf=2 ad='int((nf+1)/2) * W/nf * 0.29'
+ as='int((nf+2)/2) * W/nf * 0.29' pd='2*int((nf+1)/2) * (W/nf + 0.29)' ps='2*int((nf+2)/2) * (W/nf + 0.29)'
+ nrd='0.29 / W' nrs='0.29 / W' sa=0 sb=0 sd=0 mult=1 m=1
XM37 VOUT- V_b_2nd_stage GNDA GNDA sky130_fd_pr__nfet_01v8 L=0.6 W=28 nf=1 ad='int((nf+1)/2) * W/nf * 0.29'
+ as='int((nf+2)/2) * W/nf * 0.29' pd='2*int((nf+1)/2) * (W/nf + 0.29)' ps='2*int((nf+2)/2) * (W/nf + 0.29)'
+ nrd='0.29 / W' nrs='0.29 / W' sa=0 sb=0 sd=0 mult=1 m=1
XM38 VOUT+ V_b_2nd_stage GNDA GNDA sky130_fd_pr__nfet_01v8 L=0.6 W=28 nf=1 ad='int((nf+1)/2) * W/nf * 0.29'
+ as='int((nf+2)/2) * W/nf * 0.29' pd='2*int((nf+1)/2) * (W/nf + 0.29)' ps='2*int((nf+2)/2) * (W/nf + 0.29)'
+ nrd='0.29 / W' nrs='0.29 / W' sa=0 sb=0 sd=0 mult=1 m=1
XM39 VOUT- X VDDA VDDA sky130_fd_pr__pfet_01v8 L=0.15 W=60 nf=1 ad='int((nf+1)/2) * W/nf * 0.29' as='int((nf+2)/2) * W/nf * 0.29'
+ pd='2*int((nf+1)/2) * (W/nf + 0.29)' ps='2*int((nf+2)/2) * (W/nf + 0.29)' nrd='0.29 / W' nrs='0.29 / W'
+ sa=0 sb=0 sd=0 mult=1 m=1
XM40 VOUT+ Y VDDA VDDA sky130_fd_pr__pfet_01v8 L=0.15 W=60 nf=1 ad='int((nf+1)/2) * W/nf * 0.29' as='int((nf+2)/2) * W/nf * 0.29'
+ pd='2*int((nf+1)/2) * (W/nf + 0.29)' ps='2*int((nf+2)/2) * (W/nf + 0.29)' nrd='0.29 / W' nrs='0.29 / W'
+ sa=0 sb=0 sd=0 mult=1 m=1
XR22 VOUT- V_b_2nd_stage GNDA sky130_fd_pr__res_xhigh_po_0p35 L=5.25 mult=1 m=1
XR23 VOUT+ V_b_2nd_stage GNDA sky130_fd_pr__res_xhigh_po_0p35 L=5.25 mult=1 m=1
XM41 V_p err_amp_out GNDA GNDA sky130_fd_pr__nfet_01v8 L=0.15 W=2.5 nf=1 ad='int((nf+1)/2) * W/nf * 0.29'
+ as='int((nf+2)/2) * W/nf * 0.29' pd='2*int((nf+1)/2) * (W/nf + 0.29)' ps='2*int((nf+2)/2) * (W/nf + 0.29)'
+ nrd='0.29 / W' nrs='0.29 / W' sa=0 sb=0 sd=0 mult=1 m=1
XM5 Vb2 Vb2 VDDA VDDA sky130_fd_pr__pfet_01v8 L=0.2 W=0.63 nf=1 ad='int((nf+1)/2) * W/nf * 0.29' as='int((nf+2)/2) * W/nf * 0.29'
+ pd='2*int((nf+1)/2) * (W/nf + 0.29)' ps='2*int((nf+2)/2) * (W/nf + 0.29)' nrd='0.29 / W' nrs='0.29 / W'
+ sa=0 sb=0 sd=0 mult=1 m=1
XM6 Vb3 Vb2 Vb2_Vb3 Vb2_Vb3 sky130_fd_pr__pfet_01v8 L=0.2 W=3.6 nf=1 ad='int((nf+1)/2) * W/nf * 0.29'
+ as='int((nf+2)/2) * W/nf * 0.29' pd='2*int((nf+1)/2) * (W/nf + 0.29)' ps='2*int((nf+2)/2) * (W/nf + 0.29)'
+ nrd='0.29 / W' nrs='0.29 / W' sa=0 sb=0 sd=0 mult=1 m=1
XM43 Vb2_Vb3 Vb3 VDDA VDDA sky130_fd_pr__pfet_01v8 L=0.2 W=3.2 nf=1 ad='int((nf+1)/2) * W/nf * 0.29'
+ as='int((nf+2)/2) * W/nf * 0.29' pd='2*int((nf+1)/2) * (W/nf + 0.29)' ps='2*int((nf+2)/2) * (W/nf + 0.29)'
+ nrd='0.29 / W' nrs='0.29 / W' sa=0 sb=0 sd=0 mult=1 m=1
XC6 VOUT+ cap_res_Y sky130_fd_pr__cap_mim_m3_1 W=2 L=2 MF=138 m=138
XC7 VOUT- cap_res_X sky130_fd_pr__cap_mim_m3_1 W=2 L=2 MF=138 m=138
XM1 VDDA VDDA VDDA VDDA sky130_fd_pr__pfet_01v8 L=0.2 W=0.63 nf=1 ad='int((nf+1)/2) * W/nf * 0.29' as='int((nf+2)/2) * W/nf * 0.29'
+ pd='2*int((nf+1)/2) * (W/nf + 0.29)' ps='2*int((nf+2)/2) * (W/nf + 0.29)' nrd='0.29 / W' nrs='0.29 / W'
+ sa=0 sb=0 sd=0 mult=1 m=1
XM2 Vb2 VDDA VDDA VDDA sky130_fd_pr__pfet_01v8 L=0.2 W=0.63 nf=1 ad='int((nf+1)/2) * W/nf * 0.29' as='int((nf+2)/2) * W/nf * 0.29'
+ pd='2*int((nf+1)/2) * (W/nf + 0.29)' ps='2*int((nf+2)/2) * (W/nf + 0.29)' nrd='0.29 / W' nrs='0.29 / W'
+ sa=0 sb=0 sd=0 mult=1 m=1
XM3 Vb2_Vb3 VDDA VDDA VDDA sky130_fd_pr__pfet_01v8 L=0.2 W=1.6 nf=2 ad='int((nf+1)/2) * W/nf * 0.29'
+ as='int((nf+2)/2) * W/nf * 0.29' pd='2*int((nf+1)/2) * (W/nf + 0.29)' ps='2*int((nf+2)/2) * (W/nf + 0.29)'
+ nrd='0.29 / W' nrs='0.29 / W' sa=0 sb=0 sd=0 mult=1 m=1
XM4 Vb3 Vb2_Vb3 Vb2_Vb3 Vb2_Vb3 sky130_fd_pr__pfet_01v8 L=0.2 W=1.2 nf=2 ad='int((nf+1)/2) * W/nf * 0.29'
+ as='int((nf+2)/2) * W/nf * 0.29' pd='2*int((nf+1)/2) * (W/nf + 0.29)' ps='2*int((nf+2)/2) * (W/nf + 0.29)'
+ nrd='0.29 / W' nrs='0.29 / W' sa=0 sb=0 sd=0 mult=1 m=1
XM21 GNDA GNDA GNDA GNDA sky130_fd_pr__nfet_01v8 L=0.15 W=2.5 nf=1 ad='int((nf+1)/2) * W/nf * 0.29' as='int((nf+2)/2) * W/nf * 0.29'
+ pd='2*int((nf+1)/2) * (W/nf + 0.29)' ps='2*int((nf+2)/2) * (W/nf + 0.29)' nrd='0.29 / W' nrs='0.29 / W'
+ sa=0 sb=0 sd=0 mult=1 m=1
XM22 V_p GNDA GNDA GNDA sky130_fd_pr__nfet_01v8 L=0.15 W=2.5 nf=1 ad='int((nf+1)/2) * W/nf * 0.29' as='int((nf+2)/2) * W/nf * 0.29'
+ pd='2*int((nf+1)/2) * (W/nf + 0.29)' ps='2*int((nf+2)/2) * (W/nf + 0.29)' nrd='0.29 / W' nrs='0.29 / W'
+ sa=0 sb=0 sd=0 mult=1 m=1
XM23 V_tail_gate GNDA GNDA GNDA sky130_fd_pr__nfet_01v8 L=0.15 W=3.0 nf=2 ad='int((nf+1)/2) * W/nf * 0.29'
+ as='int((nf+2)/2) * W/nf * 0.29' pd='2*int((nf+1)/2) * (W/nf + 0.29)' ps='2*int((nf+2)/2) * (W/nf + 0.29)'
+ nrd='0.29 / W' nrs='0.29 / W' sa=0 sb=0 sd=0 mult=1 m=1
XM24 VD1 GNDA GNDA GNDA sky130_fd_pr__nfet_01v8 L=0.15 W=3.0 nf=2 ad='int((nf+1)/2) * W/nf * 0.29' as='int((nf+2)/2) * W/nf * 0.29'
+ pd='2*int((nf+1)/2) * (W/nf + 0.29)' ps='2*int((nf+2)/2) * (W/nf + 0.29)' nrd='0.29 / W' nrs='0.29 / W'
+ sa=0 sb=0 sd=0 mult=1 m=1
XM46 VD2 GNDA GNDA GNDA sky130_fd_pr__nfet_01v8 L=0.15 W=3.0 nf=2 ad='int((nf+1)/2) * W/nf * 0.29' as='int((nf+2)/2) * W/nf * 0.29'
+ pd='2*int((nf+1)/2) * (W/nf + 0.29)' ps='2*int((nf+2)/2) * (W/nf + 0.29)' nrd='0.29 / W' nrs='0.29 / W'
+ sa=0 sb=0 sd=0 mult=1 m=1
XM47 Y GNDA GNDA GNDA sky130_fd_pr__nfet_01v8 L=0.15 W=3.0 nf=2 ad='int((nf+1)/2) * W/nf * 0.29' as='int((nf+2)/2) * W/nf * 0.29'
+ pd='2*int((nf+1)/2) * (W/nf + 0.29)' ps='2*int((nf+2)/2) * (W/nf + 0.29)' nrd='0.29 / W' nrs='0.29 / W'
+ sa=0 sb=0 sd=0 mult=1 m=1
XM48 VD3 VDDA VDDA VDDA sky130_fd_pr__pfet_01v8 L=0.2 W=7.0 nf=2 ad='int((nf+1)/2) * W/nf * 0.29' as='int((nf+2)/2) * W/nf * 0.29'
+ pd='2*int((nf+1)/2) * (W/nf + 0.29)' ps='2*int((nf+2)/2) * (W/nf + 0.29)' nrd='0.29 / W' nrs='0.29 / W'
+ sa=0 sb=0 sd=0 mult=1 m=1
XM49 Y VD4 VD4 VD4 sky130_fd_pr__pfet_01v8 L=0.2 W=7.0 nf=2 ad='int((nf+1)/2) * W/nf * 0.29' as='int((nf+2)/2) * W/nf * 0.29'
+ pd='2*int((nf+1)/2) * (W/nf + 0.29)' ps='2*int((nf+2)/2) * (W/nf + 0.29)' nrd='0.29 / W' nrs='0.29 / W'
+ sa=0 sb=0 sd=0 mult=1 m=1
XM52 X VD3 VD3 VD3 sky130_fd_pr__pfet_01v8 L=0.2 W=7.0 nf=2 ad='int((nf+1)/2) * W/nf * 0.29' as='int((nf+2)/2) * W/nf * 0.29'
+ pd='2*int((nf+1)/2) * (W/nf + 0.29)' ps='2*int((nf+2)/2) * (W/nf + 0.29)' nrd='0.29 / W' nrs='0.29 / W'
+ sa=0 sb=0 sd=0 mult=1 m=1
XM58 V_err_p VDDA VDDA VDDA sky130_fd_pr__pfet_01v8 L=0.15 W=1.0 nf=2 ad='int((nf+1)/2) * W/nf * 0.29'
+ as='int((nf+2)/2) * W/nf * 0.29' pd='2*int((nf+1)/2) * (W/nf + 0.29)' ps='2*int((nf+2)/2) * (W/nf + 0.29)'
+ nrd='0.29 / W' nrs='0.29 / W' sa=0 sb=0 sd=0 mult=1 m=1
XM59 err_amp_out VDDA VDDA VDDA sky130_fd_pr__pfet_01v8 L=0.15 W=0.5 nf=1 ad='int((nf+1)/2) * W/nf * 0.29'
+ as='int((nf+2)/2) * W/nf * 0.29' pd='2*int((nf+1)/2) * (W/nf + 0.29)' ps='2*int((nf+2)/2) * (W/nf + 0.29)'
+ nrd='0.29 / W' nrs='0.29 / W' sa=0 sb=0 sd=0 mult=1 m=1
XM60 V_err_gate VDDA VDDA VDDA sky130_fd_pr__pfet_01v8 L=0.15 W=1.0 nf=2 ad='int((nf+1)/2) * W/nf * 0.29'
+ as='int((nf+2)/2) * W/nf * 0.29' pd='2*int((nf+1)/2) * (W/nf + 0.29)' ps='2*int((nf+2)/2) * (W/nf + 0.29)'
+ nrd='0.29 / W' nrs='0.29 / W' sa=0 sb=0 sd=0 mult=1 m=1
XM61 err_amp_mir VDDA VDDA VDDA sky130_fd_pr__pfet_01v8 L=0.15 W=0.5 nf=1 ad='int((nf+1)/2) * W/nf * 0.29'
+ as='int((nf+2)/2) * W/nf * 0.29' pd='2*int((nf+1)/2) * (W/nf + 0.29)' ps='2*int((nf+2)/2) * (W/nf + 0.29)'
+ nrd='0.29 / W' nrs='0.29 / W' sa=0 sb=0 sd=0 mult=1 m=1
XM62 GNDA VDDA VDDA VDDA sky130_fd_pr__pfet_01v8 L=0.15 W=4 nf=2 ad='int((nf+1)/2) * W/nf * 0.29' as='int((nf+2)/2) * W/nf * 0.29'
+ pd='2*int((nf+1)/2) * (W/nf + 0.29)' ps='2*int((nf+2)/2) * (W/nf + 0.29)' nrd='0.29 / W' nrs='0.29 / W'
+ sa=0 sb=0 sd=0 mult=1 m=1
XM63 GNDA VDDA VDDA VDDA sky130_fd_pr__pfet_01v8 L=0.15 W=4 nf=2 ad='int((nf+1)/2) * W/nf * 0.29' as='int((nf+2)/2) * W/nf * 0.29'
+ pd='2*int((nf+1)/2) * (W/nf + 0.29)' ps='2*int((nf+2)/2) * (W/nf + 0.29)' nrd='0.29 / W' nrs='0.29 / W'
+ sa=0 sb=0 sd=0 mult=1 m=1
XM64 VDDA GNDA GNDA GNDA sky130_fd_pr__nfet_01v8 L=0.15 W=6 nf=2 ad='int((nf+1)/2) * W/nf * 0.29' as='int((nf+2)/2) * W/nf * 0.29'
+ pd='2*int((nf+1)/2) * (W/nf + 0.29)' ps='2*int((nf+2)/2) * (W/nf + 0.29)' nrd='0.29 / W' nrs='0.29 / W'
+ sa=0 sb=0 sd=0 mult=1 m=1
XM65 VDDA GNDA GNDA GNDA sky130_fd_pr__nfet_01v8 L=0.15 W=6 nf=2 ad='int((nf+1)/2) * W/nf * 0.29' as='int((nf+2)/2) * W/nf * 0.29'
+ pd='2*int((nf+1)/2) * (W/nf + 0.29)' ps='2*int((nf+2)/2) * (W/nf + 0.29)' nrd='0.29 / W' nrs='0.29 / W'
+ sa=0 sb=0 sd=0 mult=1 m=1
XM66 VOUT+ GNDA GNDA GNDA sky130_fd_pr__nfet_01v8 L=0.6 W=14 nf=2 ad='int((nf+1)/2) * W/nf * 0.29' as='int((nf+2)/2) * W/nf * 0.29'
+ pd='2*int((nf+1)/2) * (W/nf + 0.29)' ps='2*int((nf+2)/2) * (W/nf + 0.29)' nrd='0.29 / W' nrs='0.29 / W'
+ sa=0 sb=0 sd=0 mult=1 m=1
XM68 VOUT- VDDA VDDA VDDA sky130_fd_pr__pfet_01v8 L=0.15 W=12 nf=2 ad='int((nf+1)/2) * W/nf * 0.29' as='int((nf+2)/2) * W/nf * 0.29'
+ pd='2*int((nf+1)/2) * (W/nf + 0.29)' ps='2*int((nf+2)/2) * (W/nf + 0.29)' nrd='0.29 / W' nrs='0.29 / W'
+ sa=0 sb=0 sd=0 mult=1 m=1
XM69 VOUT- GNDA GNDA GNDA sky130_fd_pr__nfet_01v8 L=0.6 W=14 nf=2 ad='int((nf+1)/2) * W/nf * 0.29' as='int((nf+2)/2) * W/nf * 0.29'
+ pd='2*int((nf+1)/2) * (W/nf + 0.29)' ps='2*int((nf+2)/2) * (W/nf + 0.29)' nrd='0.29 / W' nrs='0.29 / W'
+ sa=0 sb=0 sd=0 mult=1 m=1
XM67 VOUT+ VDDA VDDA VDDA sky130_fd_pr__pfet_01v8 L=0.15 W=12 nf=2 ad='int((nf+1)/2) * W/nf * 0.29' as='int((nf+2)/2) * W/nf * 0.29'
+ pd='2*int((nf+1)/2) * (W/nf + 0.29)' ps='2*int((nf+2)/2) * (W/nf + 0.29)' nrd='0.29 / W' nrs='0.29 / W'
+ sa=0 sb=0 sd=0 mult=1 m=1
XR1 cap_res_X X GNDA sky130_fd_pr__res_high_po_1p41 L=1.41 mult=1 m=1
XR2 cap_res_Y Y GNDA sky130_fd_pr__res_high_po_1p41 L=1.41 mult=1 m=1
XM20 err_amp_mir GNDA GNDA GNDA sky130_fd_pr__nfet_01v8 L=0.15 W=0.5 nf=1 ad='int((nf+1)/2) * W/nf * 0.29'
+ as='int((nf+2)/2) * W/nf * 0.29' pd='2*int((nf+1)/2) * (W/nf + 0.29)' ps='2*int((nf+2)/2) * (W/nf + 0.29)'
+ nrd='0.29 / W' nrs='0.29 / W' sa=0 sb=0 sd=0 mult=1 m=1
XM42 err_amp_out GNDA GNDA GNDA sky130_fd_pr__nfet_01v8 L=0.15 W=0.5 nf=1 ad='int((nf+1)/2) * W/nf * 0.29'
+ as='int((nf+2)/2) * W/nf * 0.29' pd='2*int((nf+1)/2) * (W/nf + 0.29)' ps='2*int((nf+2)/2) * (W/nf + 0.29)'
+ nrd='0.29 / W' nrs='0.29 / W' sa=0 sb=0 sd=0 mult=1 m=1
XM44 X GNDA GNDA GNDA sky130_fd_pr__nfet_01v8 L=0.15 W=3.0 nf=2 ad='int((nf+1)/2) * W/nf * 0.29' as='int((nf+2)/2) * W/nf * 0.29'
+ pd='2*int((nf+1)/2) * (W/nf + 0.29)' ps='2*int((nf+2)/2) * (W/nf + 0.29)' nrd='0.29 / W' nrs='0.29 / W'
+ sa=0 sb=0 sd=0 mult=1 m=1
XM45 VD4 VDDA VDDA VDDA sky130_fd_pr__pfet_01v8 L=0.2 W=7.0 nf=2 ad='int((nf+1)/2) * W/nf * 0.29' as='int((nf+2)/2) * W/nf * 0.29'
+ pd='2*int((nf+1)/2) * (W/nf + 0.29)' ps='2*int((nf+2)/2) * (W/nf + 0.29)' nrd='0.29 / W' nrs='0.29 / W'
+ sa=0 sb=0 sd=0 mult=1 m=1
XM50 GNDA GNDA GNDA GNDA sky130_fd_pr__nfet_01v8 L=0.15 W=1.5 nf=1 ad='int((nf+1)/2) * W/nf * 0.29' as='int((nf+2)/2) * W/nf * 0.29'
+ pd='2*int((nf+1)/2) * (W/nf + 0.29)' ps='2*int((nf+2)/2) * (W/nf + 0.29)' nrd='0.29 / W' nrs='0.29 / W'
+ sa=0 sb=0 sd=0 mult=1 m=1
.ends


* expanding   symbol:
*+  /foss/designs/my_design/projects/bandgapref/xschem_ngspice/new_files/opamp_bandgap_2.sym # of pins=5
** sym_path: projects/bandgapref/xschem_ngspice/new_files/opamp_bandgap_2.sym
** sch_path: projects/bandgapref/xschem_ngspice/new_files/opamp_bandgap_2.sch
.subckt opamp_bandgap_2 VDDA Vout Vin- Vin+ GNDA
*.ipin Vin+
*.opin Vout
*.ipin Vin-
*.ipin GNDA
*.ipin VDDA
XM1 V_p VDDA GNDA GNDA sky130_fd_pr__nfet_01v8 L=5 W=2.5 nf=1 ad='int((nf+1)/2) * W/nf * 0.29' as='int((nf+2)/2) * W/nf * 0.29'
+ pd='2*int((nf+1)/2) * (W/nf + 0.29)' ps='2*int((nf+2)/2) * (W/nf + 0.29)' nrd='0.29 / W' nrs='0.29 / W'
+ sa=0 sb=0 sd=0 mult=1 m=1
XM2 V_mirror Vin- V_p GNDA sky130_fd_pr__nfet_01v8 L=0.2 W=2.5 nf=1 ad='int((nf+1)/2) * W/nf * 0.29'
+ as='int((nf+2)/2) * W/nf * 0.29' pd='2*int((nf+1)/2) * (W/nf + 0.29)' ps='2*int((nf+2)/2) * (W/nf + 0.29)'
+ nrd='0.29 / W' nrs='0.29 / W' sa=0 sb=0 sd=0 mult=1 m=1
XM3 1st_Vout Vin+ V_p GNDA sky130_fd_pr__nfet_01v8 L=0.2 W=2.5 nf=1 ad='int((nf+1)/2) * W/nf * 0.29'
+ as='int((nf+2)/2) * W/nf * 0.29' pd='2*int((nf+1)/2) * (W/nf + 0.29)' ps='2*int((nf+2)/2) * (W/nf + 0.29)'
+ nrd='0.29 / W' nrs='0.29 / W' sa=0 sb=0 sd=0 mult=1 m=1
XM5 V_mirror V_mirror VDDA VDDA sky130_fd_pr__pfet_01v8 L=0.2 W=6 nf=2 ad='int((nf+1)/2) * W/nf * 0.29'
+ as='int((nf+2)/2) * W/nf * 0.29' pd='2*int((nf+1)/2) * (W/nf + 0.29)' ps='2*int((nf+2)/2) * (W/nf + 0.29)'
+ nrd='0.29 / W' nrs='0.29 / W' sa=0 sb=0 sd=0 mult=1 m=1
XM6 1st_Vout V_mirror VDDA VDDA sky130_fd_pr__pfet_01v8 L=0.2 W=6 nf=2 ad='int((nf+1)/2) * W/nf * 0.29'
+ as='int((nf+2)/2) * W/nf * 0.29' pd='2*int((nf+1)/2) * (W/nf + 0.29)' ps='2*int((nf+2)/2) * (W/nf + 0.29)'
+ nrd='0.29 / W' nrs='0.29 / W' sa=0 sb=0 sd=0 mult=1 m=1
XM4 Vout VDDA GNDA GNDA sky130_fd_pr__nfet_01v8 L=5 W=2.5 nf=1 ad='int((nf+1)/2) * W/nf * 0.29' as='int((nf+2)/2) * W/nf * 0.29'
+ pd='2*int((nf+1)/2) * (W/nf + 0.29)' ps='2*int((nf+2)/2) * (W/nf + 0.29)' nrd='0.29 / W' nrs='0.29 / W'
+ sa=0 sb=0 sd=0 mult=1 m=1
XM7 Vout 1st_Vout VDDA VDDA sky130_fd_pr__pfet_01v8 L=0.2 W=6 nf=2 ad='int((nf+1)/2) * W/nf * 0.29' as='int((nf+2)/2) * W/nf * 0.29'
+ pd='2*int((nf+1)/2) * (W/nf + 0.29)' ps='2*int((nf+2)/2) * (W/nf + 0.29)' nrd='0.29 / W' nrs='0.29 / W'
+ sa=0 sb=0 sd=0 mult=1 m=1
XC1 1st_Vout cap_res sky130_fd_pr__cap_mim_m3_1 W=2 L=2 MF=20 m=20
XM8 Vout VDDA VDDA VDDA sky130_fd_pr__pfet_01v8 L=0.2 W=1 nf=1 ad='int((nf+1)/2) * W/nf * 0.29' as='int((nf+2)/2) * W/nf * 0.29'
+ pd='2*int((nf+1)/2) * (W/nf + 0.29)' ps='2*int((nf+2)/2) * (W/nf + 0.29)' nrd='0.29 / W' nrs='0.29 / W'
+ sa=0 sb=0 sd=0 mult=2 m=2
XR2 Vout cap_res GNDA sky130_fd_pr__res_high_po_0p35 L=2.05 mult=1 m=1
.ends

.GLOBAL GND
.GLOBAL VDD
.end
